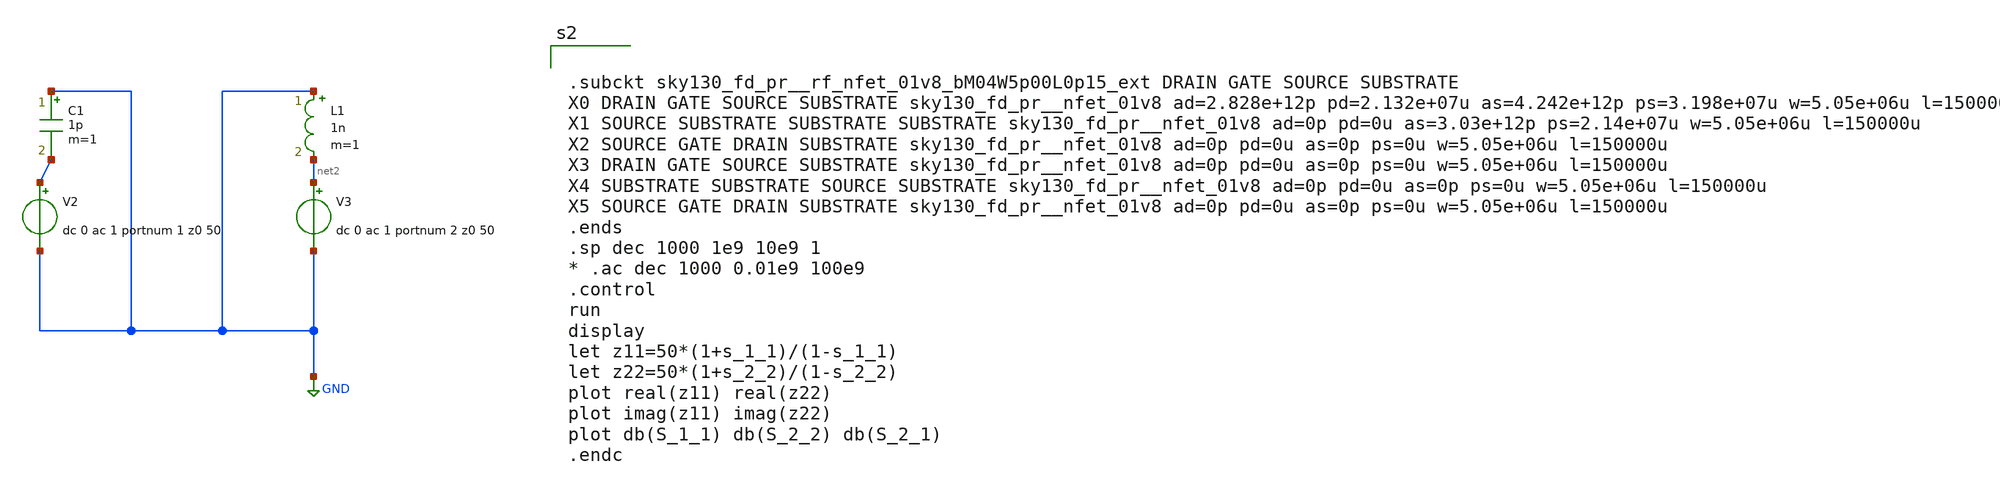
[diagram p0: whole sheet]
** sch_path: xschem/untitled-7.sch
**.subckt untitled-7
V2 net1 GND dc 0 ac 1 portnum 1 z0 50
V3 net2 GND dc 0 ac 1 portnum 2 z0 50
C1 GND net1 1p m=1
L1 GND net2 1n m=1
**** begin user architecture code
.lib $::SKYWATER_MODELS/sky130.lib.spice tt
* .include $::PDKPATH/libs.ref/sky130_fd_sc_hvl/spice/sky130_fd_sc_hvl.spice



.subckt sky130_fd_pr__rf_nfet_01v8_bM04W5p00L0p15_ext DRAIN GATE SOURCE SUBSTRATE
X0 DRAIN GATE SOURCE SUBSTRATE sky130_fd_pr__nfet_01v8 ad=2.828e+12p pd=2.132e+07u as=4.242e+12p
+ ps=3.198e+07u w=5.05e+06u l=150000u
X1 SOURCE SUBSTRATE SUBSTRATE SUBSTRATE sky130_fd_pr__nfet_01v8 ad=0p pd=0u as=3.03e+12p
+ ps=2.14e+07u w=5.05e+06u l=150000u
X2 SOURCE GATE DRAIN SUBSTRATE sky130_fd_pr__nfet_01v8 ad=0p pd=0u as=0p ps=0u w=5.05e+06u l=150000u
X3 DRAIN GATE SOURCE SUBSTRATE sky130_fd_pr__nfet_01v8 ad=0p pd=0u as=0p ps=0u w=5.05e+06u l=150000u
X4 SUBSTRATE SUBSTRATE SOURCE SUBSTRATE sky130_fd_pr__nfet_01v8 ad=0p pd=0u as=0p ps=0u w=5.05e+06u
+ l=150000u
X5 SOURCE GATE DRAIN SUBSTRATE sky130_fd_pr__nfet_01v8 ad=0p pd=0u as=0p ps=0u w=5.05e+06u l=150000u
.ends
.sp dec 1000 1e9 10e9 1
* .ac dec 1000 0.01e9 100e9
.control
run
display
let z11=50*(1+s_1_1)/(1-s_1_1)
let z22=50*(1+s_2_2)/(1-s_2_2)
plot real(z11) real(z22)
plot imag(z11) imag(z22)
plot db(S_1_1) db(S_2_2) db(S_2_1)
.endc


**** end user architecture code
**.ends
.GLOBAL GND
.end
